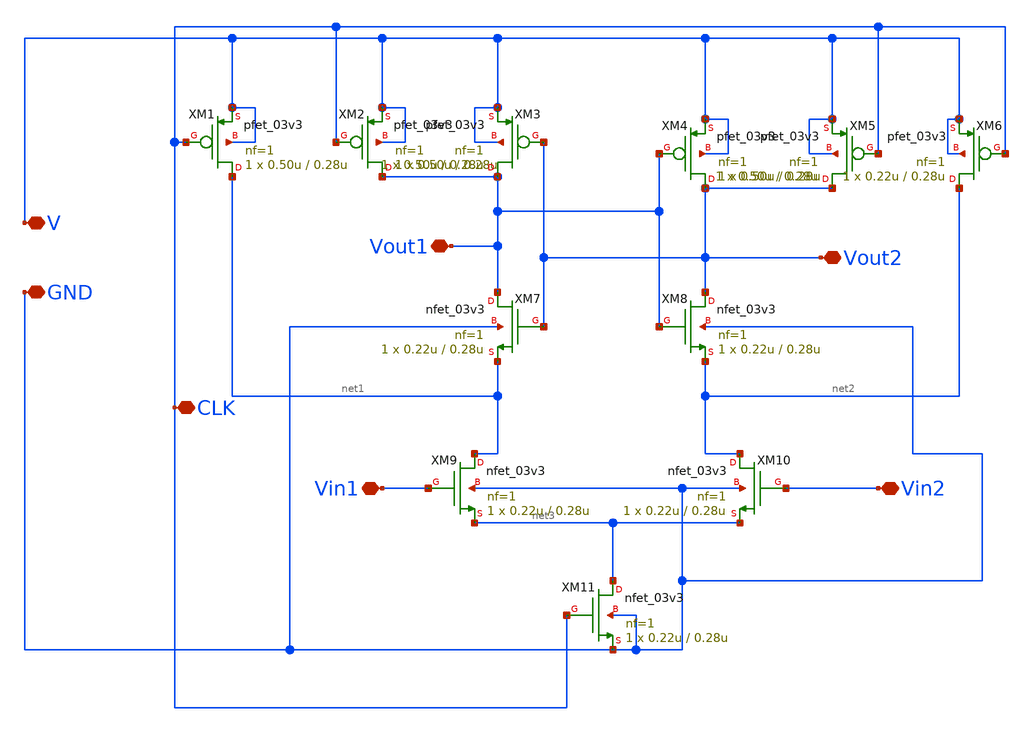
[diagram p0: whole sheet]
** sch_path: V2/Simbolos/strongarm.sch
**.subckt strongarm Vin1 GND Vout2 Vout1 Vin2 V CLK
*.iopin Vin1
*.iopin GND
*.iopin Vout2
*.iopin Vout1
*.iopin Vin2
*.iopin V
*.iopin CLK
XM1 net1 CLK V V pfet_03v3 L=0.28u W=0.50u nf=1 ad='int((nf+1)/2) * W/nf * 0.18u' as='int((nf+2)/2) * W/nf * 0.18u'
+ pd='2*int((nf+1)/2) * (W/nf + 0.18u)' ps='2*int((nf+2)/2) * (W/nf + 0.18u)' nrd='0.18u / W' nrs='0.18u / W'
+ sa=0 sb=0 sd=0 m=1
XM2 Vout1 CLK V V pfet_03v3 L=0.28u W=0.50u nf=1 ad='int((nf+1)/2) * W/nf * 0.18u' as='int((nf+2)/2) * W/nf * 0.18u'
+ pd='2*int((nf+1)/2) * (W/nf + 0.18u)' ps='2*int((nf+2)/2) * (W/nf + 0.18u)' nrd='0.18u / W' nrs='0.18u / W'
+ sa=0 sb=0 sd=0 m=1
XM3 Vout1 Vout2 V V pfet_03v3 L=0.28u W=0.50u nf=1 ad='int((nf+1)/2) * W/nf * 0.18u' as='int((nf+2)/2) * W/nf * 0.18u'
+ pd='2*int((nf+1)/2) * (W/nf + 0.18u)' ps='2*int((nf+2)/2) * (W/nf + 0.18u)' nrd='0.18u / W' nrs='0.18u / W'
+ sa=0 sb=0 sd=0 m=1
XM4 Vout2 Vout1 V V pfet_03v3 L=0.28u W=0.50u nf=1 ad='int((nf+1)/2) * W/nf * 0.18u' as='int((nf+2)/2) * W/nf * 0.18u'
+ pd='2*int((nf+1)/2) * (W/nf + 0.18u)' ps='2*int((nf+2)/2) * (W/nf + 0.18u)' nrd='0.18u / W' nrs='0.18u / W'
+ sa=0 sb=0 sd=0 m=1
XM5 Vout2 CLK V V pfet_03v3 L=0.28u W=0.50u nf=1 ad='int((nf+1)/2) * W/nf * 0.18u' as='int((nf+2)/2) * W/nf * 0.18u'
+ pd='2*int((nf+1)/2) * (W/nf + 0.18u)' ps='2*int((nf+2)/2) * (W/nf + 0.18u)' nrd='0.18u / W' nrs='0.18u / W'
+ sa=0 sb=0 sd=0 m=1
XM6 net2 CLK V V pfet_03v3 L=0.28u W=0.22u nf=1 ad='int((nf+1)/2) * W/nf * 0.18u' as='int((nf+2)/2) * W/nf * 0.18u'
+ pd='2*int((nf+1)/2) * (W/nf + 0.18u)' ps='2*int((nf+2)/2) * (W/nf + 0.18u)' nrd='0.18u / W' nrs='0.18u / W'
+ sa=0 sb=0 sd=0 m=1
XM7 Vout1 Vout2 net1 GND nfet_03v3 L=0.28u W=0.22u nf=1 ad='int((nf+1)/2) * W/nf * 0.18u' as='int((nf+2)/2) * W/nf * 0.18u'
+ pd='2*int((nf+1)/2) * (W/nf + 0.18u)' ps='2*int((nf+2)/2) * (W/nf + 0.18u)' nrd='0.18u / W' nrs='0.18u / W'
+ sa=0 sb=0 sd=0 m=1
XM8 Vout2 Vout1 net2 GND nfet_03v3 L=0.28u W=0.22u nf=1 ad='int((nf+1)/2) * W/nf * 0.18u' as='int((nf+2)/2) * W/nf * 0.18u'
+ pd='2*int((nf+1)/2) * (W/nf + 0.18u)' ps='2*int((nf+2)/2) * (W/nf + 0.18u)' nrd='0.18u / W' nrs='0.18u / W'
+ sa=0 sb=0 sd=0 m=1
XM9 net1 Vin1 net3 GND nfet_03v3 L=0.28u W=0.22u nf=1 ad='int((nf+1)/2) * W/nf * 0.18u' as='int((nf+2)/2) * W/nf * 0.18u'
+ pd='2*int((nf+1)/2) * (W/nf + 0.18u)' ps='2*int((nf+2)/2) * (W/nf + 0.18u)' nrd='0.18u / W' nrs='0.18u / W'
+ sa=0 sb=0 sd=0 m=1
XM10 net2 Vin2 net3 GND nfet_03v3 L=0.28u W=0.22u nf=1 ad='int((nf+1)/2) * W/nf * 0.18u' as='int((nf+2)/2) * W/nf * 0.18u'
+ pd='2*int((nf+1)/2) * (W/nf + 0.18u)' ps='2*int((nf+2)/2) * (W/nf + 0.18u)' nrd='0.18u / W' nrs='0.18u / W'
+ sa=0 sb=0 sd=0 m=1
XM11 net3 CLK GND GND nfet_03v3 L=0.28u W=0.22u nf=1 ad='int((nf+1)/2) * W/nf * 0.18u' as='int((nf+2)/2) * W/nf * 0.18u'
+ pd='2*int((nf+1)/2) * (W/nf + 0.18u)' ps='2*int((nf+2)/2) * (W/nf + 0.18u)' nrd='0.18u / W' nrs='0.18u / W'
+ sa=0 sb=0 sd=0 m=1
**** begin user architecture code

.include /foss/pdks/gf180mcuC/libs.tech/ngspice/design.ngspice
.lib /foss/pdks/gf180mcuC/libs.tech/ngspice/sm141064.ngspice typical

**** end user architecture code
**.ends
.end
